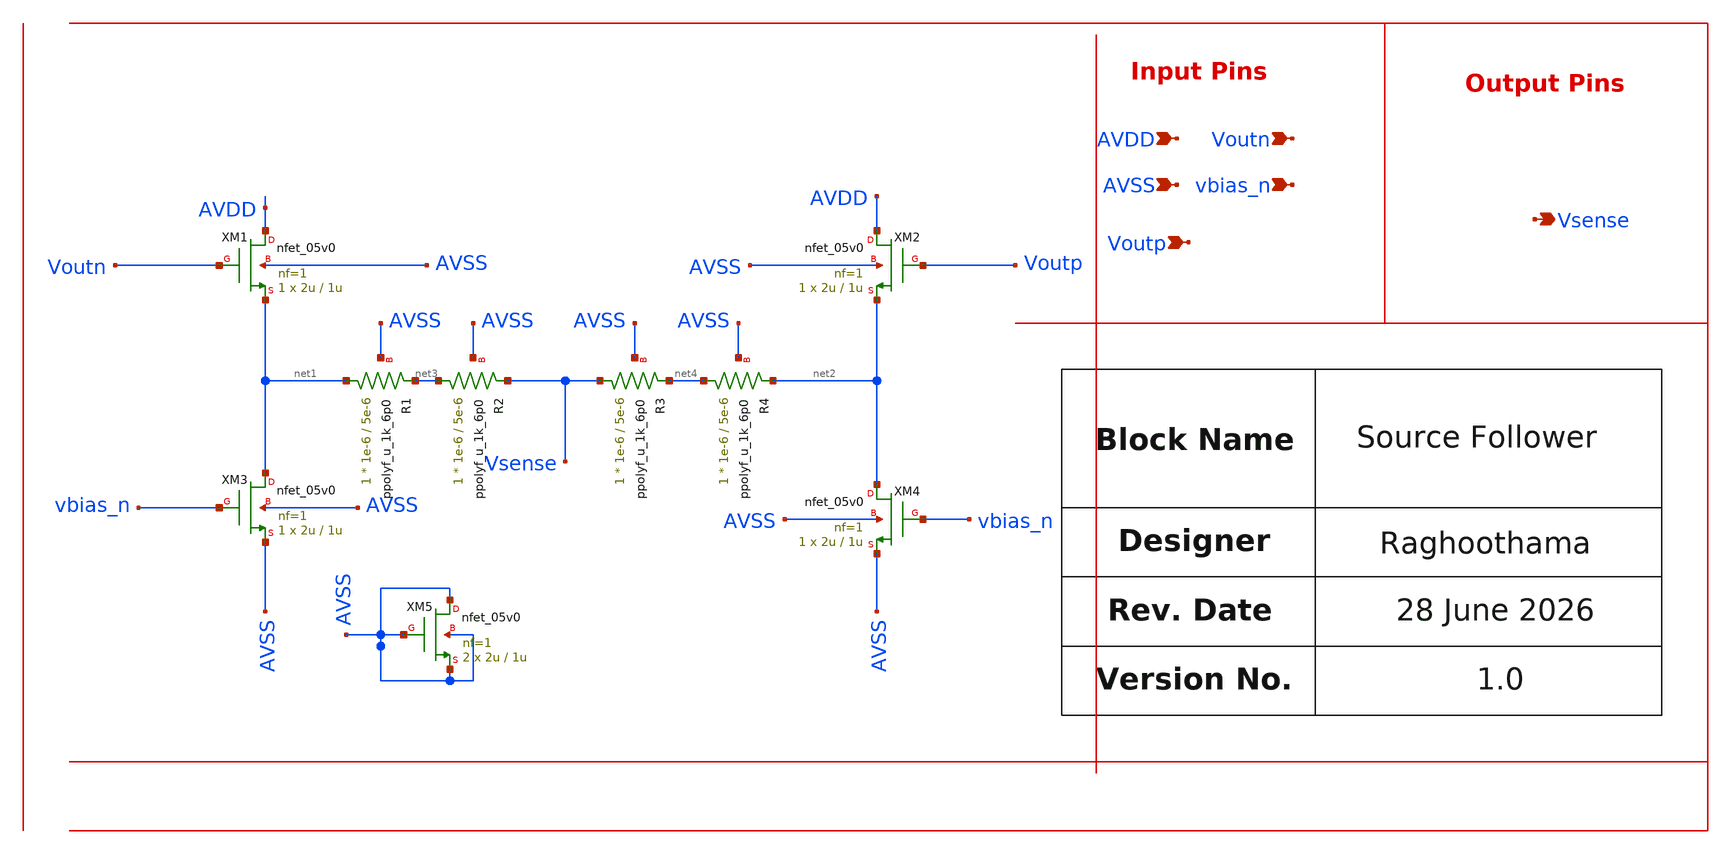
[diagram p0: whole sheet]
** sch_path: design/schematics/ADC/Adder/OTA/rrao_cic_bms_afe_ota2_source_follower.sch
**.subckt rrao_cic_bms_afe_ota2_source_follower AVSS AVDD Voutp Voutn vbias_n Vsense
*.ipin AVSS
*.ipin AVDD
*.ipin Voutp
*.ipin Voutn
*.ipin vbias_n
*.opin Vsense
XM1 AVDD Voutn net1 AVSS nfet_05v0 L=1u W=2u nf=1 ad='int((nf+1)/2) * W/nf * 0.18u' as='int((nf+2)/2) * W/nf * 0.18u'
+ pd='2*int((nf+1)/2) * (W/nf + 0.18u)' ps='2*int((nf+2)/2) * (W/nf + 0.18u)' nrd='0.18u / W' nrs='0.18u / W'
+ sa=0 sb=0 sd=0 m=1
XM3 net1 vbias_n AVSS AVSS nfet_05v0 L=1u W=2u nf=1 ad='int((nf+1)/2) * W/nf * 0.18u' as='int((nf+2)/2) * W/nf * 0.18u'
+ pd='2*int((nf+1)/2) * (W/nf + 0.18u)' ps='2*int((nf+2)/2) * (W/nf + 0.18u)' nrd='0.18u / W' nrs='0.18u / W'
+ sa=0 sb=0 sd=0 m=1
XM4 net2 vbias_n AVSS AVSS nfet_05v0 L=1u W=2u nf=1 ad='int((nf+1)/2) * W/nf * 0.18u' as='int((nf+2)/2) * W/nf * 0.18u'
+ pd='2*int((nf+1)/2) * (W/nf + 0.18u)' ps='2*int((nf+2)/2) * (W/nf + 0.18u)' nrd='0.18u / W' nrs='0.18u / W'
+ sa=0 sb=0 sd=0 m=1
XM2 AVDD Voutp net2 AVSS nfet_05v0 L=1u W=2u nf=1 ad='int((nf+1)/2) * W/nf * 0.18u' as='int((nf+2)/2) * W/nf * 0.18u'
+ pd='2*int((nf+1)/2) * (W/nf + 0.18u)' ps='2*int((nf+2)/2) * (W/nf + 0.18u)' nrd='0.18u / W' nrs='0.18u / W'
+ sa=0 sb=0 sd=0 m=1
XM5 AVSS AVSS AVSS AVSS nfet_05v0 L=1u W=2u nf=1 ad='int((nf+1)/2) * W/nf * 0.18u' as='int((nf+2)/2) * W/nf * 0.18u'
+ pd='2*int((nf+1)/2) * (W/nf + 0.18u)' ps='2*int((nf+2)/2) * (W/nf + 0.18u)' nrd='0.18u / W' nrs='0.18u / W'
+ sa=0 sb=0 sd=0 m=2
XR1 net1 net3 AVSS ppolyf_u_1k_6p0 r_width=1e-6 r_length=5e-6 m=1
XR2 net3 Vsense AVSS ppolyf_u_1k_6p0 r_width=1e-6 r_length=5e-6 m=1
XR3 Vsense net4 AVSS ppolyf_u_1k_6p0 r_width=1e-6 r_length=5e-6 m=1
XR4 net4 net2 AVSS ppolyf_u_1k_6p0 r_width=1e-6 r_length=5e-6 m=1
**.ends
.end
